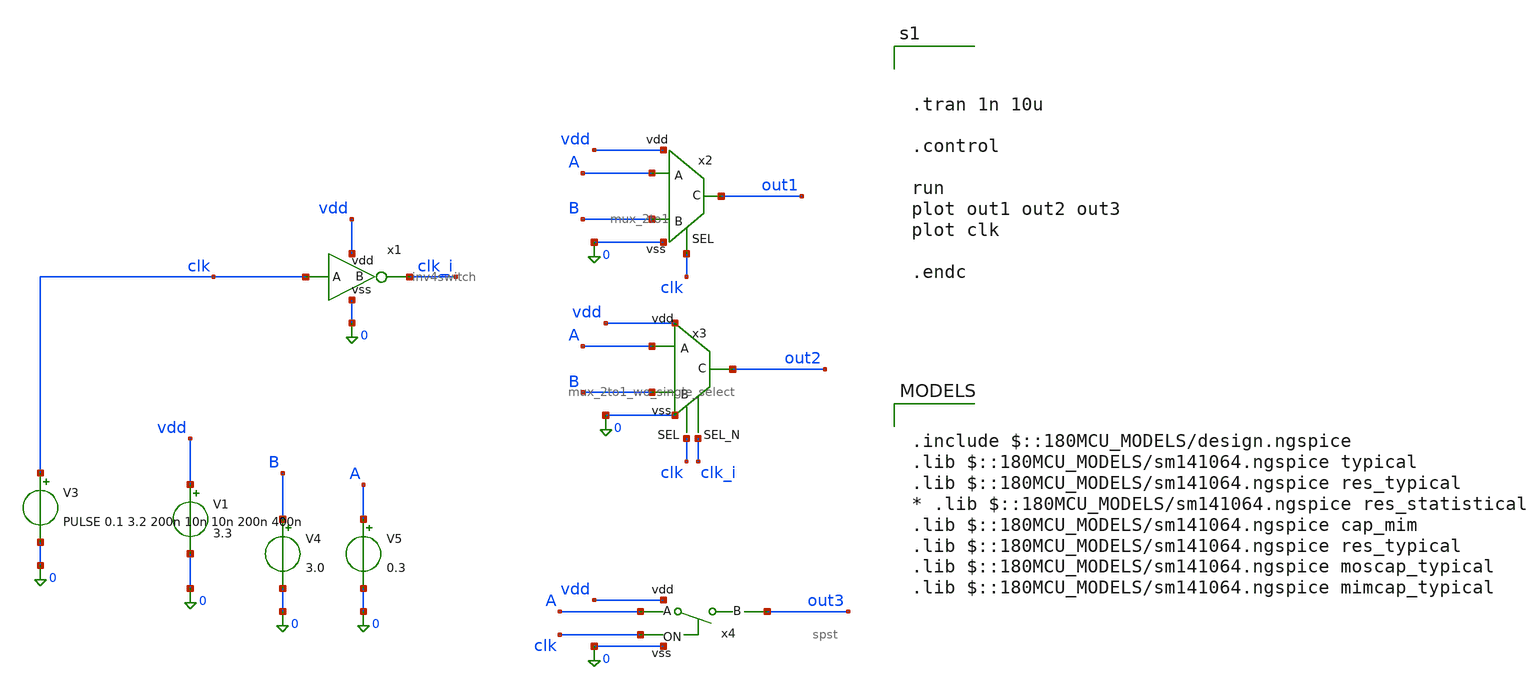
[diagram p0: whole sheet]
** sch_path: General/ADC/switching/switches_tb.sch
**.subckt switches_tb
x1 clk_i clk vdd 0 inv4switch
x2 clk A out1 B vdd 0 mux_2to1
x3 clk_i clk A out2 B vdd 0 mux_2to1_wo_single_select
x4 out3 A clk vdd 0 spst
V1 vdd 0 3.3
V3 clk 0 PULSE 0.1 3.2 200n 10n 10n 200n 400n
V4 B 0 3.0
V5 A 0 0.3
**** begin user architecture code

.include $::180MCU_MODELS/design.ngspice
.lib $::180MCU_MODELS/sm141064.ngspice typical
.lib $::180MCU_MODELS/sm141064.ngspice res_typical
* .lib $::180MCU_MODELS/sm141064.ngspice res_statistical
.lib $::180MCU_MODELS/sm141064.ngspice cap_mim
.lib $::180MCU_MODELS/sm141064.ngspice res_typical
.lib $::180MCU_MODELS/sm141064.ngspice moscap_typical
.lib $::180MCU_MODELS/sm141064.ngspice mimcap_typical




.tran 1n 10u

.control

run
plot out1 out2 out3
plot clk

.endc



**** end user architecture code
**.ends
.end
